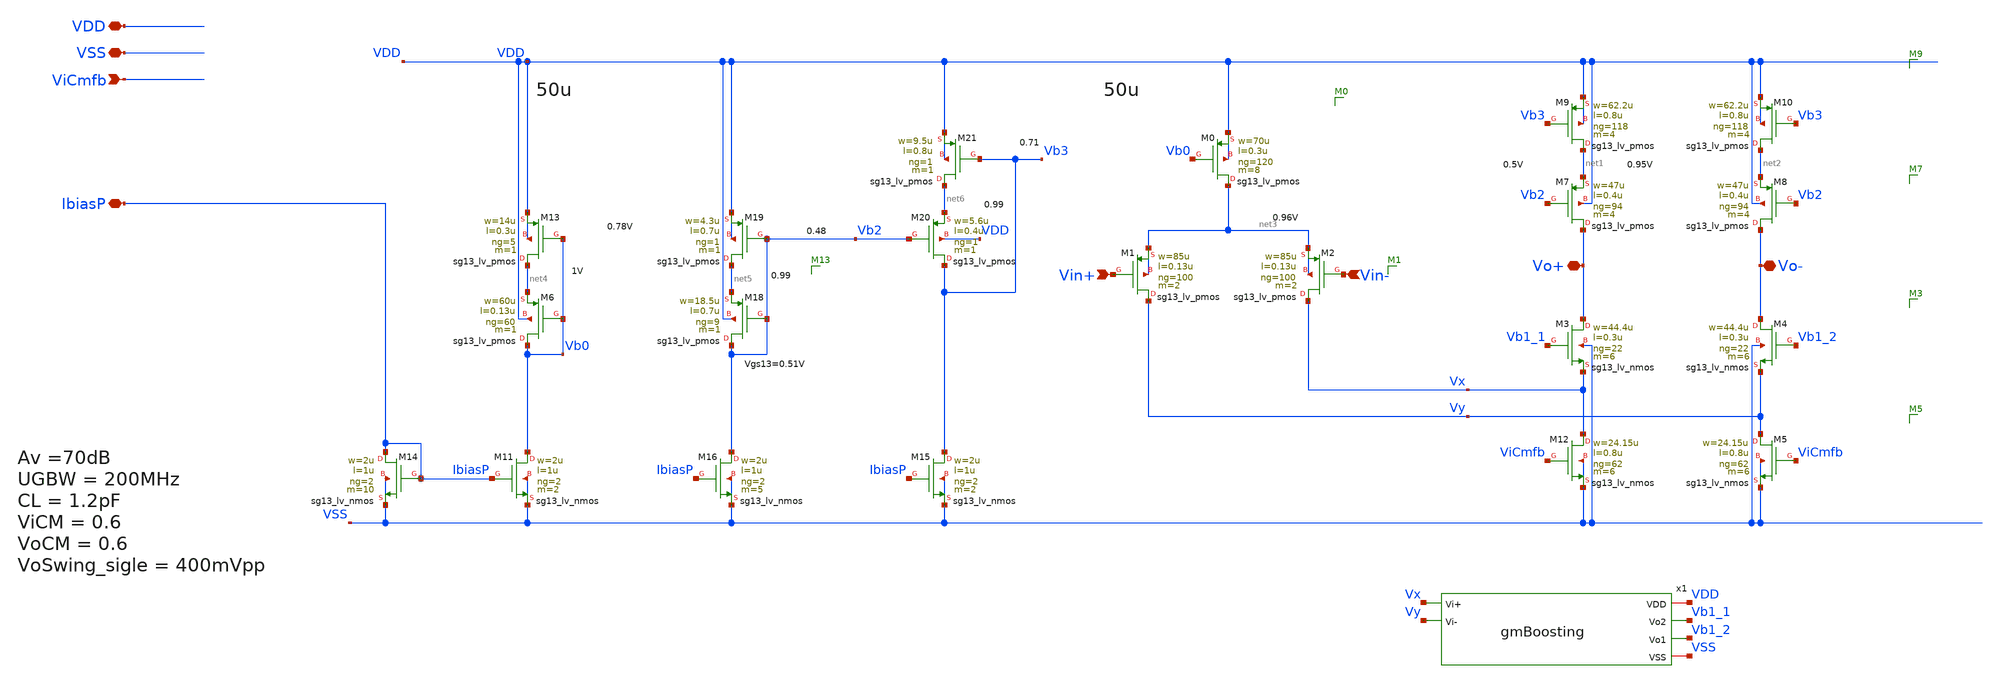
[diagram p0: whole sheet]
** sch_path: sch/blocks/foldedCascode.sch
**.subckt foldedCascode VSS VDD ViCmfb IbiasP Vin+ Vin- Vo+ Vo-
*.iopin VSS
*.iopin VDD
*.ipin ViCmfb
*.iopin IbiasP
*.ipin Vin+
*.ipin Vin-
*.iopin Vo+
*.iopin Vo-
x1 VDD Vb1_1 Vb1_2 Vx Vy VSS gmBoosting
XM0 net3 Vb0 VDD VDD sg13_lv_pmos w=70u l=0.3u ng=120 m=8 mm_ok=1
XM1 Vy Vin+ net3 net3 sg13_lv_pmos w=85u l=0.13u ng=100 m=2 mm_ok=1
XM2 Vx Vin- net3 net3 sg13_lv_pmos w=85u l=0.13u ng=100 m=2 mm_ok=1
XM7 Vo+ Vb2 net1 VDD sg13_lv_pmos w=47u l=0.4u ng=94 m=4 mm_ok=1
XM3 Vo+ Vb1_1 Vx VSS sg13_lv_nmos w=44.4u l=0.3u ng=22 m=6 mm_ok=1
XM8 Vo- Vb2 net2 VDD sg13_lv_pmos w=47u l=0.4u ng=94 m=4 mm_ok=1
XM12 Vx ViCmfb VSS VSS sg13_lv_nmos w=24.15u l=0.8u ng=62 m=6 mm_ok=1
XM4 Vo- Vb1_2 Vy VSS sg13_lv_nmos w=44.4u l=0.3u ng=22 m=6 mm_ok=1
XM5 Vy ViCmfb VSS VSS sg13_lv_nmos w=24.15u l=0.8u ng=62 m=6 mm_ok=1
XM6 Vb0 Vb0 net4 VDD sg13_lv_pmos w=60u l=0.13u ng=60 m=1 mm_ok=1
XM13 net4 Vb0 VDD VDD sg13_lv_pmos w=14u l=0.3u ng=5 m=1 mm_ok=1
XM18 Vb2 Vb2 net5 VDD sg13_lv_pmos w=18.5u l=0.7u ng=9 m=1 mm_ok=1
XM19 net5 Vb2 VDD VDD sg13_lv_pmos w=4.3u l=0.7u ng=1 m=1 mm_ok=1
XM20 Vb3 Vb2 net6 VDD sg13_lv_pmos w=5.6u l=0.4u ng=1 m=1 mm_ok=1
XM21 net6 Vb3 VDD VDD sg13_lv_pmos w=9.5u l=0.8u ng=1 m=1 mm_ok=1
XM9 net1 Vb3 VDD VDD sg13_lv_pmos w=62.2u l=0.8u ng=118 m=4 mm_ok=1
XM10 net2 Vb3 VDD VDD sg13_lv_pmos w=62.2u l=0.8u ng=118 m=4 mm_ok=1
XM14 IbiasP IbiasP VSS VSS sg13_lv_nmos w=2u l=1u ng=2 m=10 mm_ok=1
XM11 Vb0 IbiasP VSS VSS sg13_lv_nmos w=2u l=1u ng=2 m=2 mm_ok=1
XM15 Vb3 IbiasP VSS VSS sg13_lv_nmos w=2u l=1u ng=2 m=2 mm_ok=1
XM16 Vb2 IbiasP VSS VSS sg13_lv_nmos w=2u l=1u ng=2 m=5 mm_ok=1
**.ends

* expanding   symbol:  gmBoosting.sym # of pins=6
** sym_path: sch/blocks/gmBoosting.sym
** sch_path: sch/blocks/gmBoosting.sch
.subckt gmBoosting VDD Vo2 Vo1 Vi+ Vi- VSS
*.iopin VSS
*.opin Vo1
*.opin Vo2
*.ipin Vi+
*.ipin Vi-
*.iopin VDD
V1 Vref VSS 0.55
XM7 net2 Vb4 VDD VDD sg13_lv_pmos w=25u l=0.7u ng=13 m=2 mm_ok=1
XM1 net8 Vi+ net1 net1 sg13_lv_pmos w=40u l=0.15u ng=80 m=4 mm_ok=1
XM2 net4 Vi- net1 net1 sg13_lv_pmos w=40u l=0.15u ng=80 m=4 mm_ok=1
XM0 net1 Vb0 net5 VDD sg13_lv_pmos w=16u l=0.3u ng=20 m=1 mm_ok=1
XM6 net8 Vb3 VSS VSS sg13_lv_nmos w=20u l=0.7u ng=5 m=2 mm_ok=1
XM9 Vo1 Vb2 net2 VDD sg13_lv_pmos w=30u l=0.3u ng=10 m=1 mm_ok=1
XM10 Vo2 Vb2 net3 VDD sg13_lv_pmos w=30u l=0.3u ng=10 m=1 mm_ok=1
XM8 net3 Vb4 VDD VDD sg13_lv_pmos w=25u l=0.7u ng=13 m=2 mm_ok=1
XM3 net5 Vo2 VDD VDD sg13_lv_pmos w=20u l=0.13u ng=5 m=1 mm_ok=1
XM4 net5 Vo1 VDD VDD sg13_lv_pmos w=20u l=0.13u ng=5 m=1 mm_ok=1
XM5 net6 Vref VDD VDD sg13_lv_pmos w=20u l=0.13u ng=5 m=2 mm_ok=1
XM28 Vb0 net7 VSS VSS sg13_lv_nmos w=10u l=0.2u ng=2 m=1 mm_ok=1
XM29 Vb3 Vb3 VSS VSS sg13_lv_nmos w=30u l=0.2u ng=4 m=1 mm_ok=1
XR16 net7 Vb0 sub! rppd w=0.8e-6 l=2.5e-6 m=1 b=0 mm_ok=1
XM30 Vb3 Vb0 net6 VDD sg13_lv_pmos w=16u l=0.3u ng=20 m=1 mm_ok=1
XM31 net4 Vb3 VSS VSS sg13_lv_nmos w=20u l=0.7u ng=5 m=2 mm_ok=1
XM32 Vo1 Vb1 net4 VSS sg13_lv_nmos w=37.5u l=0.7u ng=5 m=1 mm_ok=1
XM33 Vo2 Vb1 net8 VSS sg13_lv_nmos w=37.5u l=0.7u ng=5 m=1 mm_ok=1
XM23 net7 Vbb VDD VDD sg13_lv_pmos w=18u l=1u ng=18 m=1 mm_ok=1
XR9 Vb1 net10 sub! rhigh w=0.5e-6 l=2.31e-6 m=1 b=0 mm_ok=1
XM17 net10 Vb1 net9 VSS sg13_lv_nmos w=25u l=0.7u ng=3 m=1 mm_ok=1
XM18 net9 net10 VSS VSS sg13_lv_nmos w=40u l=0.7u ng=4 m=1 mm_ok=1
XM19 net11 Vb4 VDD VDD sg13_lv_pmos w=15u l=0.7u ng=5 m=1 mm_ok=1
XM20 Vb4 Vb2 net11 VDD sg13_lv_pmos w=7u l=0.3u ng=7 m=1 mm_ok=1
XR10 Vb4 Vb2 sub! rhigh w=0.5e-6 l=1.8e-6 m=1 b=0 mm_ok=1
I3 Vbb VSS 50u
XM21 Vbb Vbb VDD VDD sg13_lv_pmos w=18u l=1u ng=18 m=1 mm_ok=1
XM22 Vb1 Vbb VDD VDD sg13_lv_pmos w=18u l=1u ng=18 m=1 mm_ok=1
XM24 net12 Vbb VDD VDD sg13_lv_pmos w=18u l=1u ng=18 m=1 mm_ok=1
XM25 net12 net12 VSS VSS sg13_lv_nmos w=15u l=1u ng=2 m=1 mm_ok=1
XM26 Vb2 net12 VSS VSS sg13_lv_nmos w=15u l=1u ng=2 m=1 mm_ok=1
.ends

.end
